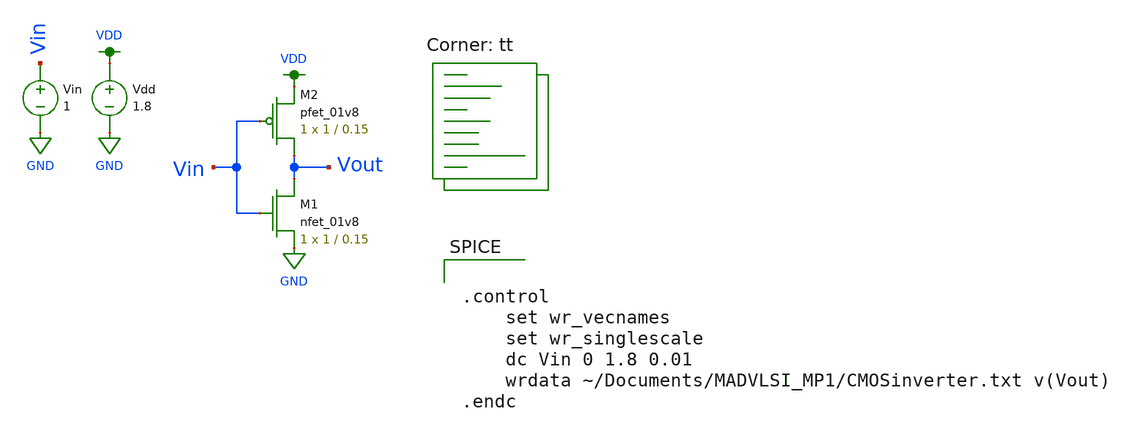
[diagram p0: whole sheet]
** sch_path: MADVLSI_MP1/CMOSinverter.sch
**.subckt CMOSinverter
XM1 Vout Vin GND GND sky130_fd_pr__nfet_01v8 L=0.15 W=1 nf=1 ad='int((nf+1)/2) * W/nf * 0.29' as='int((nf+2)/2) * W/nf * 0.29'
+ pd='2*int((nf+1)/2) * (W/nf + 0.29)' ps='2*int((nf+2)/2) * (W/nf + 0.29)' nrd='0.29 / W' nrs='0.29 / W'
+ sa=0 sb=0 sd=0 mult=1 m=1
Vdd VDD GND 1.8
XM2 Vout Vin VDD VDD sky130_fd_pr__pfet_01v8 L=0.15 W=1 nf=1 ad='int((nf+1)/2) * W/nf * 0.29' as='int((nf+2)/2) * W/nf * 0.29'
+ pd='2*int((nf+1)/2) * (W/nf + 0.29)' ps='2*int((nf+2)/2) * (W/nf + 0.29)' nrd='0.29 / W' nrs='0.29 / W'
+ sa=0 sb=0 sd=0 mult=1 m=1
Vin Vin GND 1
**** begin user architecture code


.control
	set wr_vecnames
	set wr_singlescale
	dc Vin 0 1.8 0.01
	wrdata ~/Documents/MADVLSI_MP1/CMOSinverter.txt v(Vout)
.endc

.lib $::SKYWATER_MODELS/sky130.lib.spice tt
**** end user architecture code
**.ends
.GLOBAL GND
.GLOBAL VDD
.end
